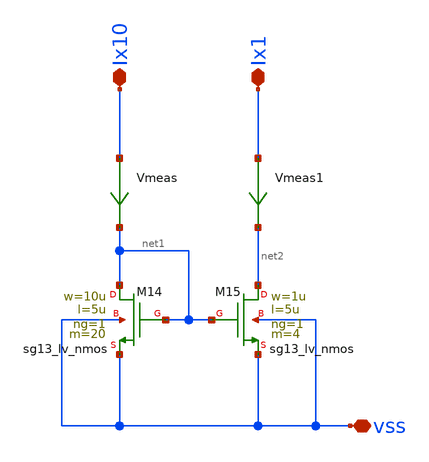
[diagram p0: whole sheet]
** sch_path: v2_feature_extr/current_mirror.sch
**.subckt current_mirror Ix10 Ix1 vss
*.iopin Ix10
*.iopin Ix1
*.iopin vss
XM14 net1 net1 vss vss sg13_lv_nmos w=10u l=5u ng=1 m=20 mm_ok=1
Vmeas Ix10 net1 0
.save i(vmeas)
XM15 net2 net1 vss vss sg13_lv_nmos w=1u l=5u ng=1 m=4 mm_ok=1
Vmeas1 Ix1 net2 0
.save i(vmeas1)
**.ends
.end
